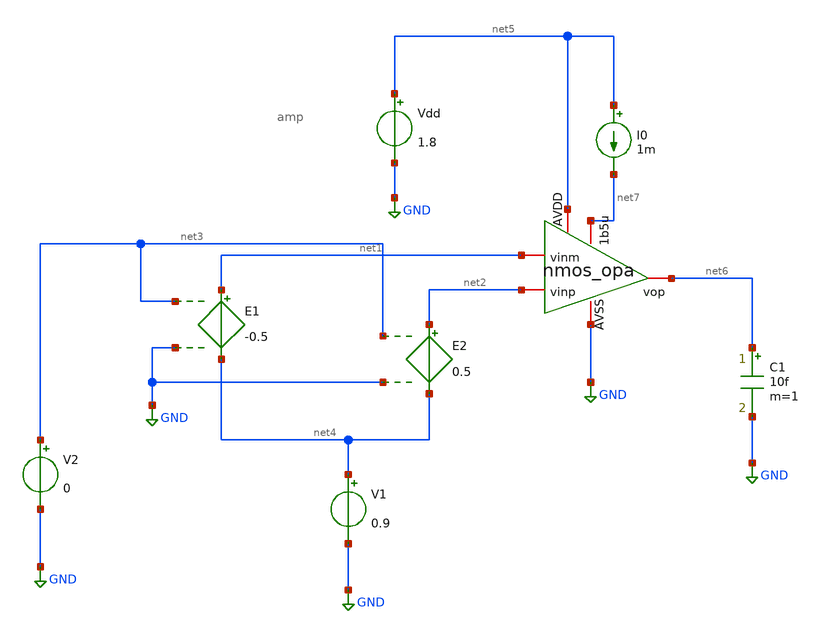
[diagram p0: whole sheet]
** sch_path: work/xschem/mic1_opamp.sch
**.subckt mic1_opamp
E1 net1 net4 net3 GND -0.5
E2 net2 net4 net3 GND 0.5
V1 net4 GND 0.9
V2 net3 GND 0
Vdd net5 GND 1.8
I0 net5 net7 1m
C1 net6 GND 10f m=1
x1 net5 net6 net1 net2 net7 GND amp
**.ends

* expanding   symbol:  amp.sym # of pins=6
** sym_path: work/xschem/amp.sym
** sch_path: work/xschem/amp.sch
.subckt amp AVDD vop vinm vinp 1b5u AVSS
*.iopin vop
*.iopin vinp
*.iopin vinm
*.iopin 1b5u
*.iopin AVSS
*.iopin AVDD
XMtail net1 1b5u AVSS AVSS sky130_fd_pr__nfet_01v8 L=1 W=5 nf=1 ad='int((1 + 1)/2) * 5 / 1 * 0.29' as='int((1 + 2)/2) * 5 / 1 * 0.29'
+ pd='2*int((1 + 1)/2) * (5 / 1 + 0.29)' ps='2*int((1 + 2)/2) * (5 / 1 + 0.29)' nrd='0.29 / 5 ' nrs='0.29 / 5 '
+ sa=0 sb=0 sd=0 mult=2 m=2
XM1 1b5u 1b5u AVSS AVSS sky130_fd_pr__nfet_01v8 L=1 W=5 nf=1 ad='int((1 + 1)/2) * 5 / 1 * 0.29' as='int((1 + 2)/2) * 5 / 1 * 0.29'
+ pd='2*int((1 + 1)/2) * (5 / 1 + 0.29)' ps='2*int((1 + 2)/2) * (5 / 1 + 0.29)' nrd='0.29 / 5 ' nrs='0.29 / 5 '
+ sa=0 sb=0 sd=0 mult=1 m=1
XMpcmm vop vom AVDD AVDD sky130_fd_pr__pfet_01v8 L=2 W=5 nf=1 ad='int((nf+1)/2) * W/nf * 0.29' as='int((nf+2)/2) * W/nf * 0.29'
+ pd='2*int((nf+1)/2) * (W/nf + 0.29)' ps='2*int((nf+2)/2) * (W/nf + 0.29)' nrd='0.29 / W' nrs='0.29 / W'
+ sa=0 sb=0 sd=0 mult=2 m=2
XMpcmp vom vom AVDD AVDD sky130_fd_pr__pfet_01v8 L=2 W=5 nf=1 ad='int((nf+1)/2) * W/nf * 0.29' as='int((nf+2)/2) * W/nf * 0.29'
+ pd='2*int((nf+1)/2) * (W/nf + 0.29)' ps='2*int((nf+2)/2) * (W/nf + 0.29)' nrd='0.29 / W' nrs='0.29 / W'
+ sa=0 sb=0 sd=0 mult=2 m=2
XMim vop vinm net1 net1 sky130_fd_pr__nfet_01v8 L=2 W=5 nf=1 ad='int((1 + 1)/2) * 5 / 1 * 0.29' as='int((1 + 2)/2) * 5 / 1 * 0.29'
+ pd='2*int((1 + 1)/2) * (5 / 1 + 0.29)' ps='2*int((1 + 2)/2) * (5 / 1 + 0.29)' nrd='0.29 / 5 ' nrs='0.29 / 5 '
+ sa=0 sb=0 sd=0 mult=4 m=4
XMip vom vinp net1 net1 sky130_fd_pr__nfet_01v8 L=2 W=5 nf=1 ad='int((1 + 1)/2) * 5 / 1 * 0.29' as='int((1 + 2)/2) * 5 / 1 * 0.29'
+ pd='2*int((1 + 1)/2) * (5 / 1 + 0.29)' ps='2*int((1 + 2)/2) * (5 / 1 + 0.29)' nrd='0.29 / 5 ' nrs='0.29 / 5 '
+ sa=0 sb=0 sd=0 mult=4 m=4
**** begin user architecture code



* ngspice commands
.control
save all
write amp.raw
set appendfile
write amp.raw

.endc



**** end user architecture code
.ends

.GLOBAL GND
.end
